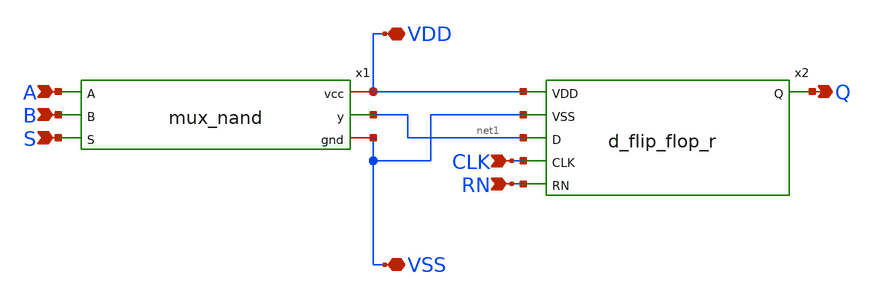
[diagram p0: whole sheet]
** sch_path: designs/libs/sdffrq_nand_toplevel/sdffrq_var_nand_toplevel.sch
**.subckt sdffrq_var_nand_toplevel A B S Q VDD VSS RN CLK
*.ipin A
*.ipin B
*.ipin S
*.opin Q
*.iopin VDD
*.iopin VSS
*.ipin RN
*.ipin CLK
x1 VDD A net1 B S VSS mux_nand
x2 VDD VSS Q net1 CLK RN d_flip_flop_r
**.ends
.end
